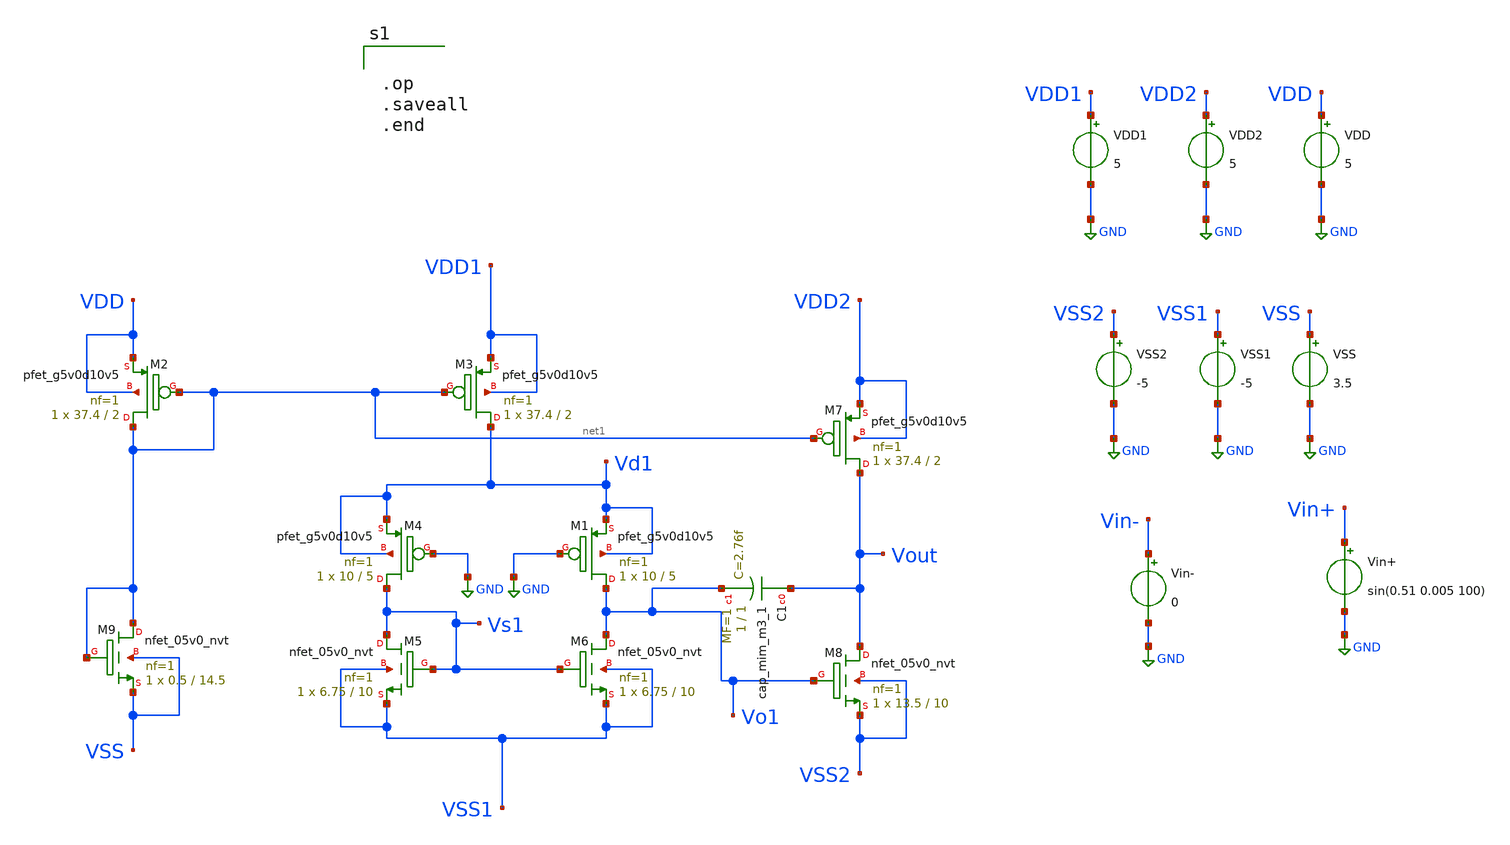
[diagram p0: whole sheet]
** sch_path: OpAmp.sch
**.subckt OpAmp
XM2 net1 net1 VDD VDD sky130_fd_pr__pfet_g5v0d10v5 L=2 W=37.4 nf=1 ad='int((1 + 1)/2) * 37.4 / 1 * 0.29'
+ as='int((1 + 2)/2) * 37.4 / 1 * 0.29' pd='2*int((1 + 1)/2) * (37.4 / 1 + 0.29)' ps='2*int((1 + 2)/2) * (37.4 / 1 + 0.29)'
+ nrd='0.29 / 37.4 ' nrs='0.29 / 37.4 ' sa=0 sb=0 sd=0 mult=1 m=1
XM3 Vd1 net1 VDD1 VDD1 sky130_fd_pr__pfet_g5v0d10v5 L=2 W=37.4 nf=1 ad='int((1 + 1)/2) * 37.4 / 1 * 0.29'
+ as='int((1 + 2)/2) * 37.4 / 1 * 0.29' pd='2*int((1 + 1)/2) * (37.4 / 1 + 0.29)' ps='2*int((1 + 2)/2) * (37.4 / 1 + 0.29)'
+ nrd='0.29 / 37.4 ' nrs='0.29 / 37.4 ' sa=0 sb=0 sd=0 mult=1 m=1
XM5 Vs1 Vs1 VSS1 VSS1 sky130_fd_pr__nfet_05v0_nvt L=10 W=6.75 nf=1 ad='int((1 + 1)/2) * 6.75 / 1 * 0.29'
+ as='int((1 + 2)/2) * 6.75 / 1 * 0.29' pd='2*int((1 + 1)/2) * (6.75 / 1 + 0.29)' ps='2*int((1 + 2)/2) * (6.75 / 1 + 0.29)'
+ nrd='0.29 / 6.75 ' nrs='0.29 / 6.75 ' sa=0 sb=0 sd=0 mult=1 m=1
XM6 Vo1 Vs1 VSS1 VSS1 sky130_fd_pr__nfet_05v0_nvt L=10 W=6.75 nf=1 ad='int((1 + 1)/2) * 6.75 / 1 * 0.29'
+ as='int((1 + 2)/2) * 6.75 / 1 * 0.29' pd='2*int((1 + 1)/2) * (6.75 / 1 + 0.29)' ps='2*int((1 + 2)/2) * (6.75 / 1 + 0.29)'
+ nrd='0.29 / 6.75 ' nrs='0.29 / 6.75 ' sa=0 sb=0 sd=0 mult=1 m=1
XM7 Vout net1 VDD2 VDD2 sky130_fd_pr__pfet_g5v0d10v5 L=2 W=37.4 nf=1 ad='int((1 + 1)/2) * 37.4 / 1 * 0.29'
+ as='int((1 + 2)/2) * 37.4 / 1 * 0.29' pd='2*int((1 + 1)/2) * (37.4 / 1 + 0.29)' ps='2*int((1 + 2)/2) * (37.4 / 1 + 0.29)'
+ nrd='0.29 / 37.4 ' nrs='0.29 / 37.4 ' sa=0 sb=0 sd=0 mult=1 m=1
XM8 Vout Vo1 VSS2 VSS2 sky130_fd_pr__nfet_05v0_nvt L=10 W=13.5 nf=1 ad='int((1 + 1)/2) * 13.5 / 1 * 0.29'
+ as='int((1 + 2)/2) * 13.5 / 1 * 0.29' pd='2*int((1 + 1)/2) * (13.5 / 1 + 0.29)' ps='2*int((1 + 2)/2) * (13.5 / 1 + 0.29)'
+ nrd='0.29 / 13.5 ' nrs='0.29 / 13.5 ' sa=0 sb=0 sd=0 mult=1 m=1
VDD VDD GND 5
Vin+ Vin+ GND sin(0.51 0.005 100)
VSS VSS GND 3.5
Vin- Vin- GND 0
VDD1 VDD1 GND 5
VDD2 VDD2 GND 5
VSS1 VSS1 GND -5
VSS2 VSS2 GND -5
XC1 Vout Vo1 sky130_fd_pr__cap_mim_m3_1 W=1 L=1 MF=1 m=1
XM1 Vo1 GND Vd1 Vd1 sky130_fd_pr__pfet_g5v0d10v5 L=5 W=10 nf=1 ad='int((1 + 1)/2) * 10 / 1 * 0.29' as='int((1 + 2)/2) * 10 / 1 * 0.29'
+ pd='2*int((1 + 1)/2) * (10 / 1 + 0.29)' ps='2*int((1 + 2)/2) * (10 / 1 + 0.29)' nrd='0.29 / 10 ' nrs='0.29 / 10 '
+ sa=0 sb=0 sd=0 mult=1 m=1
XM4 Vs1 GND Vd1 Vd1 sky130_fd_pr__pfet_g5v0d10v5 L=5 W=10 nf=1 ad='int((1 + 1)/2) * 10 / 1 * 0.29' as='int((1 + 2)/2) * 10 / 1 * 0.29'
+ pd='2*int((1 + 1)/2) * (10 / 1 + 0.29)' ps='2*int((1 + 2)/2) * (10 / 1 + 0.29)' nrd='0.29 / 10 ' nrs='0.29 / 10 '
+ sa=0 sb=0 sd=0 mult=1 m=1
XM9 net1 net1 VSS VSS sky130_fd_pr__nfet_05v0_nvt L=14.5 W=0.5 nf=1 ad='int((1 + 1)/2) * 0.5 / 1 * 0.29'
+ as='int((1 + 2)/2) * 0.5 / 1 * 0.29' pd='2*int((1 + 1)/2) * (0.5 / 1 + 0.29)' ps='2*int((1 + 2)/2) * (0.5 / 1 + 0.29)'
+ nrd='0.29 / 0.5 ' nrs='0.29 / 0.5 ' sa=0 sb=0 sd=0 mult=1 m=1
**** begin user architecture code


.op
.saveall
.end


** opencircuitdesign pdks install
.lib $::SKYWATER_MODELS/sky130.lib.spice tt

**** end user architecture code
**.ends
.GLOBAL GND
.end
